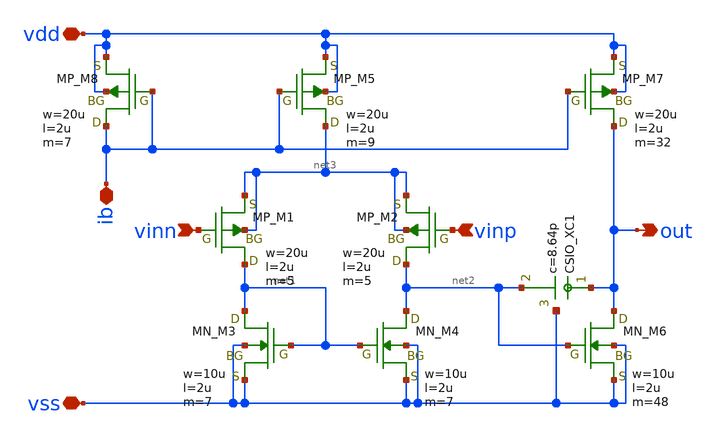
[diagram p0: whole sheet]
** sch_path: member_project/DCDC/xschem/opamp_ramp.sch
**.subckt opamp_ramp vdd vss vinn vinp out ib
*.iopin vdd
*.iopin vss
*.ipin vinn
*.ipin vinp
*.opin out
*.iopin ib
XM1 net1 vinn net3 net3 PMOS w=20u l=2u as=0 ad=0 ps=0 pd=0 nrd=0 nrs=0 m=5
XM2 net2 vinp net3 net3 PMOS w=20u l=2u as=0 ad=0 ps=0 pd=0 nrd=0 nrs=0 m=5
XM3 net1 net1 vss vss NMOS w=10u l=2u as=0 ad=0 ps=0 pd=0 nrd=0 nrs=0 m=7
XM4 net2 net1 vss vss NMOS w=10u l=2u as=0 ad=0 ps=0 pd=0 nrd=0 nrs=0 m=7
XM5 net3 ib vdd vdd PMOS w=20u l=2u as=0 ad=0 ps=0 pd=0 nrd=0 nrs=0 m=9
XM7 out ib vdd vdd PMOS w=20u l=2u as=0 ad=0 ps=0 pd=0 nrd=0 nrs=0 m=32
XM6 out net2 vss vss NMOS w=10u l=2u as=0 ad=0 ps=0 pd=0 nrd=0 nrs=0 m=48
XM8 ib ib vdd vdd PMOS w=20u l=2u as=0 ad=0 ps=0 pd=0 nrd=0 nrs=0 m=7
XXC1 out net2 vss F_CSIO c=8.64p x=120u y=120u m=1
**.ends
.end
